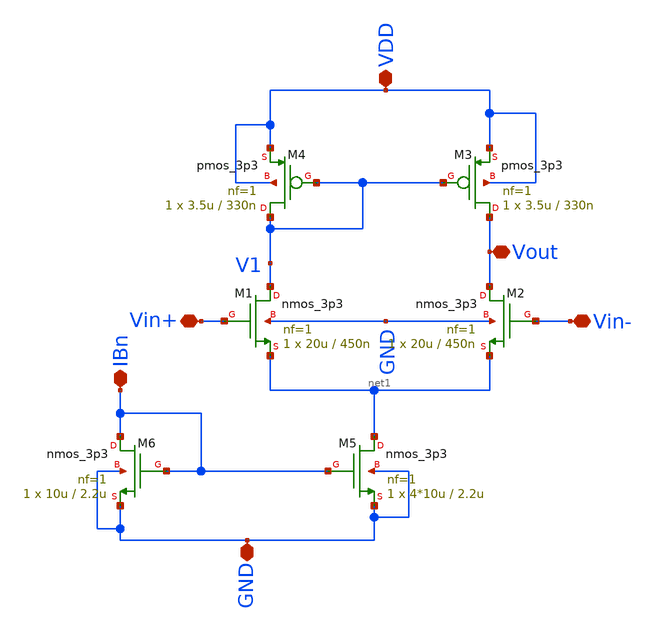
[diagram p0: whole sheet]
** sch_path: ITI_Labs/Lab7/Design/Lab07.sch
**.subckt Lab07 VDD GND IBn Vin- Vin+ Vout
*.iopin VDD
*.iopin GND
*.iopin IBn
*.iopin Vin-
*.iopin Vin+
*.iopin Vout
XM1 V1 Vin+ net1 GND nmos_3p3 L=450n W=20u nf=1 ad='int((nf+1)/2) * W/nf * 0.18u' as='int((nf+2)/2) * W/nf * 0.18u'
+ pd='2*int((nf+1)/2) * (W/nf + 0.18u)' ps='2*int((nf+2)/2) * (W/nf + 0.18u)' nrd='0.18u / W' nrs='0.18u / W'
+ sa=0 sb=0 sd=0 m=1
XM4 V1 V1 VDD VDD pmos_3p3 L=330n W=3.5u nf=1 ad='int((nf+1)/2) * W/nf * 0.18u' as='int((nf+2)/2) * W/nf * 0.18u'
+ pd='2*int((nf+1)/2) * (W/nf + 0.18u)' ps='2*int((nf+2)/2) * (W/nf + 0.18u)' nrd='0.18u / W' nrs='0.18u / W'
+ sa=0 sb=0 sd=0 m=1
XM5 net1 IBn GND GND nmos_3p3 L=2.2u W=4*10u nf=1 ad='int((nf+1)/2) * W/nf * 0.18u' as='int((nf+2)/2) * W/nf * 0.18u'
+ pd='2*int((nf+1)/2) * (W/nf + 0.18u)' ps='2*int((nf+2)/2) * (W/nf + 0.18u)' nrd='0.18u / W' nrs='0.18u / W'
+ sa=0 sb=0 sd=0 m=1
XM6 IBn IBn GND GND nmos_3p3 L=2.2u W=10u nf=1 ad='int((nf+1)/2) * W/nf * 0.18u' as='int((nf+2)/2) * W/nf * 0.18u'
+ pd='2*int((nf+1)/2) * (W/nf + 0.18u)' ps='2*int((nf+2)/2) * (W/nf + 0.18u)' nrd='0.18u / W' nrs='0.18u / W'
+ sa=0 sb=0 sd=0 m=1
XM3 Vout V1 VDD VDD pmos_3p3 L=330n W=3.5u nf=1 ad='int((nf+1)/2) * W/nf * 0.18u' as='int((nf+2)/2) * W/nf * 0.18u'
+ pd='2*int((nf+1)/2) * (W/nf + 0.18u)' ps='2*int((nf+2)/2) * (W/nf + 0.18u)' nrd='0.18u / W' nrs='0.18u / W'
+ sa=0 sb=0 sd=0 m=1
XM2 Vout Vin- net1 GND nmos_3p3 L=450n W=20u nf=1 ad='int((nf+1)/2) * W/nf * 0.18u' as='int((nf+2)/2) * W/nf * 0.18u'
+ pd='2*int((nf+1)/2) * (W/nf + 0.18u)' ps='2*int((nf+2)/2) * (W/nf + 0.18u)' nrd='0.18u / W' nrs='0.18u / W'
+ sa=0 sb=0 sd=0 m=1
**.ends
.end
